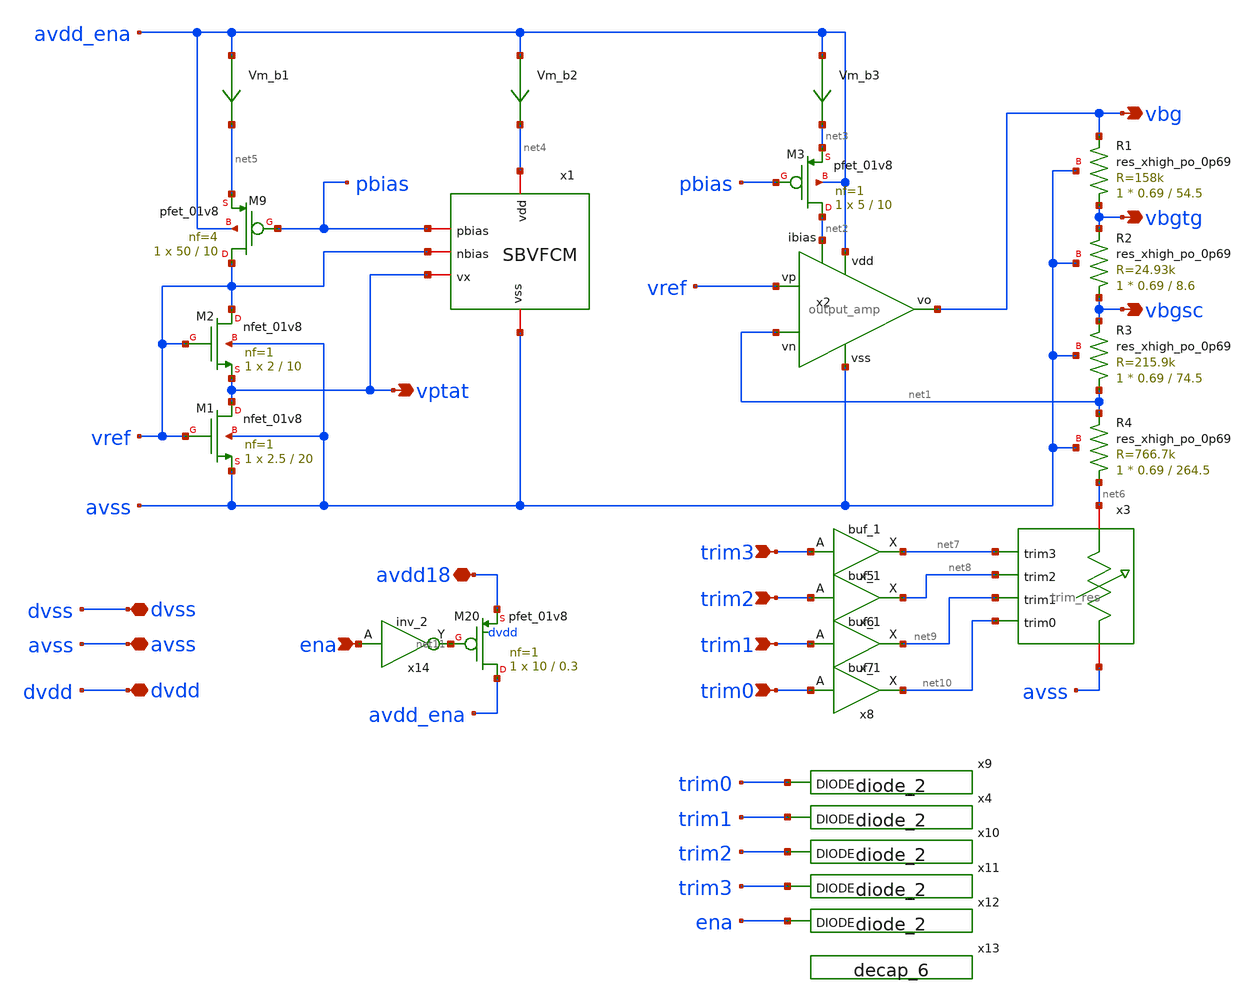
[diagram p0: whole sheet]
** sch_path: xschem/sky130_ak_ip__cmos_vref.sch
**.subckt sky130_ak_ip__cmos_vref vbg avss avdd18 dvss ena vbgsc vbgtg trim3 trim2 trim1 trim0 vptat
*+ dvdd
*.opin vbg
*.iopin avss
*.iopin avdd18
*.iopin dvss
*.ipin ena
*.opin vbgsc
*.opin vbgtg
*.ipin trim3
*.ipin trim2
*.ipin trim1
*.ipin trim0
*.opin vptat
*.iopin dvdd
XM2 vref vref vptat avss sky130_fd_pr__nfet_01v8 L=10 W=2 nf=1 ad='int((nf+1)/2) * W/nf * 0.29' as='int((nf+2)/2) * W/nf * 0.29'
+ pd='2*int((nf+1)/2) * (W/nf + 0.29)' ps='2*int((nf+2)/2) * (W/nf + 0.29)' nrd='0.29 / W' nrs='0.29 / W'
+ sa=0 sb=0 sd=0 mult=1 m=1
XM1 vptat vref avss avss sky130_fd_pr__nfet_01v8 L=20 W=2.5 nf=1 ad='int((nf+1)/2) * W/nf * 0.29' as='int((nf+2)/2) * W/nf * 0.29'
+ pd='2*int((nf+1)/2) * (W/nf + 0.29)' ps='2*int((nf+2)/2) * (W/nf + 0.29)' nrd='0.29 / W' nrs='0.29 / W'
+ sa=0 sb=0 sd=0 mult=1 m=1
XM9 vref pbias net5 avdd_ena sky130_fd_pr__pfet_01v8 L=10 W=50 nf=4 ad='int((nf+1)/2) * W/nf * 0.29'
+ as='int((nf+2)/2) * W/nf * 0.29' pd='2*int((nf+1)/2) * (W/nf + 0.29)' ps='2*int((nf+2)/2) * (W/nf + 0.29)'
+ nrd='0.29 / W' nrs='0.29 / W' sa=0 sb=0 sd=0 mult=1 m=1
XM20 avdd_ena net11 avdd18 dvdd sky130_fd_pr__pfet_01v8 L=0.3 W=10 nf=1 ad='int((nf+1)/2) * W/nf * 0.29'
+ as='int((nf+2)/2) * W/nf * 0.29' pd='2*int((nf+1)/2) * (W/nf + 0.29)' ps='2*int((nf+2)/2) * (W/nf + 0.29)'
+ nrd='0.29 / W' nrs='0.29 / W' sa=0 sb=0 sd=0 mult=1 m=1
x1 net4 pbias vref vptat avss sbvfcm
x2 avdd_ena vbg vref net1 net2 avss output_amp
XM3 net2 pbias net3 avdd_ena sky130_fd_pr__pfet_01v8 L=10 W=5 nf=1 ad='int((nf+1)/2) * W/nf * 0.29' as='int((nf+2)/2) * W/nf * 0.29'
+ pd='2*int((nf+1)/2) * (W/nf + 0.29)' ps='2*int((nf+2)/2) * (W/nf + 0.29)' nrd='0.29 / W' nrs='0.29 / W'
+ sa=0 sb=0 sd=0 mult=1 m=1
Vm_b1 avdd_ena net5 0
.save i(vm_b1)
Vm_b2 avdd_ena net4 0
.save i(vm_b2)
Vm_b3 avdd_ena net3 0
.save i(vm_b3)
x3 net6 net10 net8 net7 net9 avss trim_res
XR4 net6 net1 avss sky130_fd_pr__res_xhigh_po_0p69 L=264.5 mult=1 m=1
XR3 net1 vbgsc avss sky130_fd_pr__res_xhigh_po_0p69 L=74.5 mult=1 m=1
XR2 vbgsc vbgtg avss sky130_fd_pr__res_xhigh_po_0p69 L=8.6 mult=1 m=1
XR1 vbgtg vbg avss sky130_fd_pr__res_xhigh_po_0p69 L=54.5 mult=1 m=1
x5 trim3 dvss dvss dvdd dvdd net7 sky130_fd_sc_hd__buf_1
x6 trim2 dvss dvss dvdd dvdd net8 sky130_fd_sc_hd__buf_1
x7 trim1 dvss dvss dvdd dvdd net9 sky130_fd_sc_hd__buf_1
x8 trim0 dvss dvss dvdd dvdd net10 sky130_fd_sc_hd__buf_1
x9 trim0 dvss dvss dvdd dvdd sky130_fd_sc_hd__diode_2
x14 ena dvss dvss dvdd dvdd net11 sky130_fd_sc_hd__inv_2
x4 trim1 dvss dvss dvdd dvdd sky130_fd_sc_hd__diode_2
x10 trim2 dvss dvss dvdd dvdd sky130_fd_sc_hd__diode_2
x11 trim3 dvss dvss dvdd dvdd sky130_fd_sc_hd__diode_2
x12 ena dvss dvss dvdd dvdd sky130_fd_sc_hd__diode_2
x13 dvss dvss dvdd dvdd sky130_fd_sc_hd__decap_6
**.ends
.end
